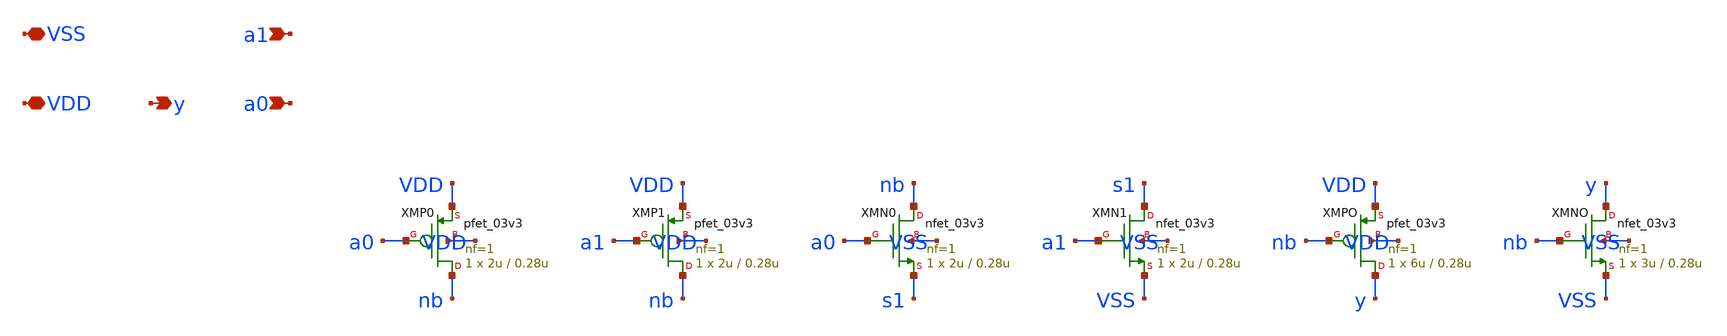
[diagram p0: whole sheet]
** sch_path: design/rowdrv.sch
**.subckt rowdrv a0 a1 y VDD VSS
*.ipin a0
*.ipin a1
*.opin y
*.iopin VDD
*.iopin VSS
XMP0 nb a0 VDD VDD pfet_03v3 L=0.28u W=2u nf=1 ad='int((nf+1)/2) * W/nf * 0.18u' as='int((nf+2)/2) * W/nf * 0.18u'
+ pd='2*int((nf+1)/2) * (W/nf + 0.18u)' ps='2*int((nf+2)/2) * (W/nf + 0.18u)' nrd='0.18u / W' nrs='0.18u / W'
+ sa=0 sb=0 sd=0 m=1
XMP1 nb a1 VDD VDD pfet_03v3 L=0.28u W=2u nf=1 ad='int((nf+1)/2) * W/nf * 0.18u' as='int((nf+2)/2) * W/nf * 0.18u'
+ pd='2*int((nf+1)/2) * (W/nf + 0.18u)' ps='2*int((nf+2)/2) * (W/nf + 0.18u)' nrd='0.18u / W' nrs='0.18u / W'
+ sa=0 sb=0 sd=0 m=1
XMN0 nb a0 s1 VSS nfet_03v3 L=0.28u W=2u nf=1 ad='int((nf+1)/2) * W/nf * 0.18u' as='int((nf+2)/2) * W/nf * 0.18u'
+ pd='2*int((nf+1)/2) * (W/nf + 0.18u)' ps='2*int((nf+2)/2) * (W/nf + 0.18u)' nrd='0.18u / W' nrs='0.18u / W'
+ sa=0 sb=0 sd=0 m=1
XMN1 s1 a1 VSS VSS nfet_03v3 L=0.28u W=2u nf=1 ad='int((nf+1)/2) * W/nf * 0.18u' as='int((nf+2)/2) * W/nf * 0.18u'
+ pd='2*int((nf+1)/2) * (W/nf + 0.18u)' ps='2*int((nf+2)/2) * (W/nf + 0.18u)' nrd='0.18u / W' nrs='0.18u / W'
+ sa=0 sb=0 sd=0 m=1
XMPO y nb VDD VDD pfet_03v3 L=0.28u W=6u nf=1 ad='int((nf+1)/2) * W/nf * 0.18u' as='int((nf+2)/2) * W/nf * 0.18u'
+ pd='2*int((nf+1)/2) * (W/nf + 0.18u)' ps='2*int((nf+2)/2) * (W/nf + 0.18u)' nrd='0.18u / W' nrs='0.18u / W'
+ sa=0 sb=0 sd=0 m=1
XMNO y nb VSS VSS nfet_03v3 L=0.28u W=3u nf=1 ad='int((nf+1)/2) * W/nf * 0.18u' as='int((nf+2)/2) * W/nf * 0.18u'
+ pd='2*int((nf+1)/2) * (W/nf + 0.18u)' ps='2*int((nf+2)/2) * (W/nf + 0.18u)' nrd='0.18u / W' nrs='0.18u / W'
+ sa=0 sb=0 sd=0 m=1
**.ends
.end
